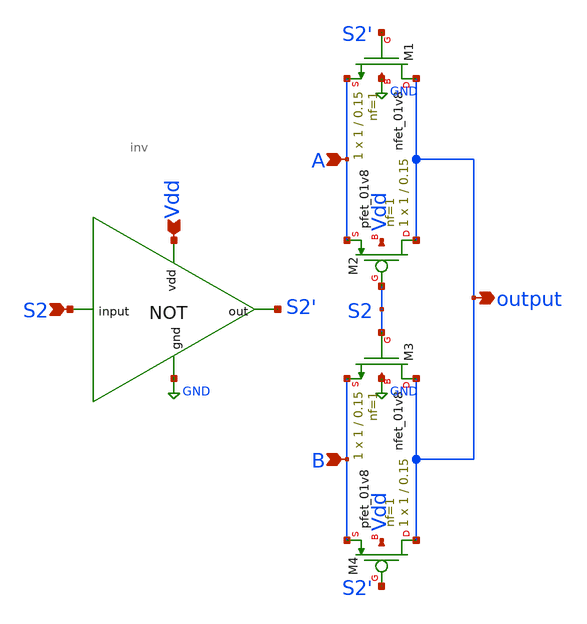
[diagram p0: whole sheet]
** sch_path: schematics/mux2to1.sch
**.subckt mux2to1 output A B S2 Vdd
*.opin output
*.ipin A
*.ipin B
*.ipin S2
*.ipin Vdd
XM1 output S2' A GND sky130_fd_pr__nfet_01v8 L=0.15 W=1 nf=1 ad='int((1 + 1)/2) * 1 / 1 * 0.29' as='int((1
+ + 2)/2) * 1 / 1 * 0.29' pd='2*int((1 + 1)/2) * (1 / 1 + 0.29)' ps='2*int((1 + 2)/2) * (1 / 1 + 0.29)' nrd='0.29
+ / 1 ' nrs='0.29 / 1 ' sa=0 sb=0 sd=0 mult=1 m=1
XM2 output S2 A Vdd sky130_fd_pr__pfet_01v8 L=0.15 W=1 nf=1 ad='int((1 + 1)/2) * 1 / 1 * 0.29' as='int((1
+ + 2)/2) * 1 / 1 * 0.29' pd='2*int((1 + 1)/2) * (1 / 1 + 0.29)' ps='2*int((1 + 2)/2) * (1 / 1 + 0.29)' nrd='0.29
+ / 1 ' nrs='0.29 / 1 ' sa=0 sb=0 sd=0 mult=1 m=1
XM3 output S2 B GND sky130_fd_pr__nfet_01v8 L=0.15 W=1 nf=1 ad='int((1 + 1)/2) * 1 / 1 * 0.29' as='int((1
+ + 2)/2) * 1 / 1 * 0.29' pd='2*int((1 + 1)/2) * (1 / 1 + 0.29)' ps='2*int((1 + 2)/2) * (1 / 1 + 0.29)' nrd='0.29
+ / 1 ' nrs='0.29 / 1 ' sa=0 sb=0 sd=0 mult=1 m=1
XM4 output S2' B Vdd sky130_fd_pr__pfet_01v8 L=0.15 W=1 nf=1 ad='int((1 + 1)/2) * 1 / 1 * 0.29' as='int((1 + 2)/2) * 1 / 1 * 0.29'
+ pd='2*int((1 + 1)/2) * (1 / 1 + 0.29)' ps='2*int((1 + 2)/2) * (1 / 1 + 0.29)' nrd='0.29 / 1 ' nrs='0.29 / 1 '
+ sa=0 sb=0 sd=0 mult=1 m=1
x1 S2' Vdd S2 GND inv
**.ends
.GLOBAL GND
.end
